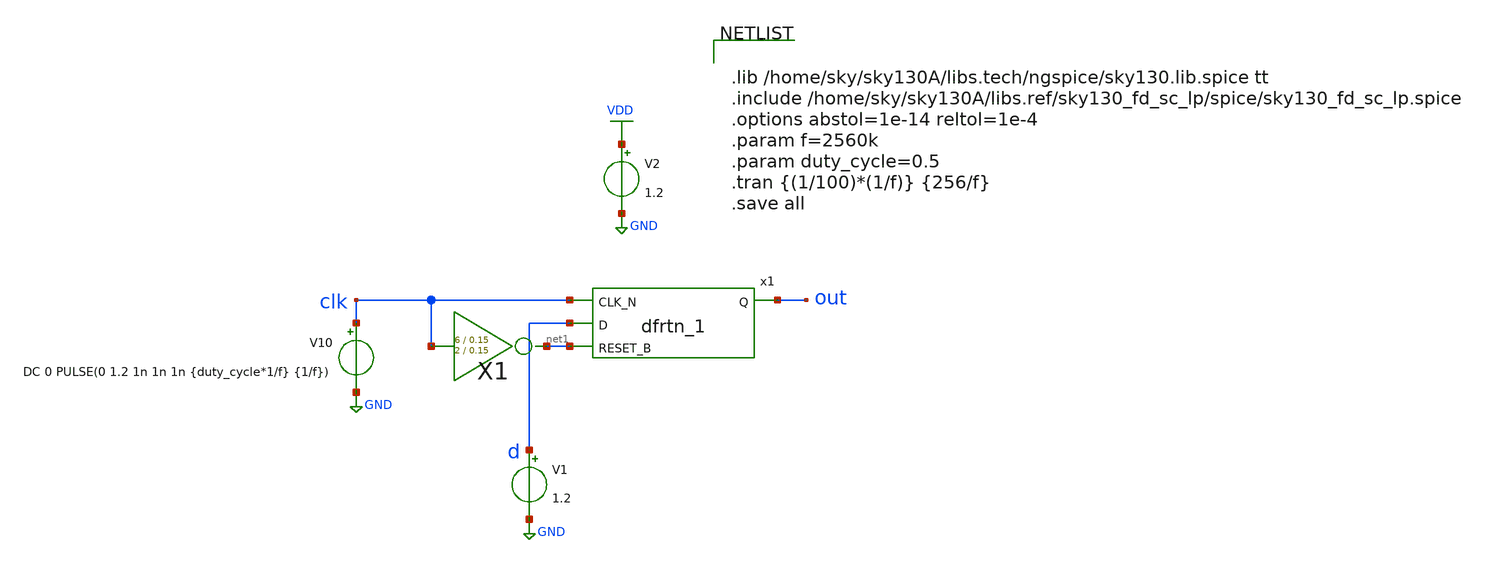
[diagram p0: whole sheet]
** sch_path: xschem/readout/test_flop.sch
**.subckt test_flop
V2 VDD GND 1.2
V10 clk GND DC 0 PULSE(0 1.2 1n 1n 1n {duty_cycle*1/f} {1/f})
V1 d GND 1.2
x1 clk d net1 GND GND VDD VDD out sky130_fd_sc_lp__dfrtn_1
X1 clk net1 inv Wpmos=6 Lpmos=0.15 Wnmos=2 Lnmos=0.15
**** begin user architecture code


.lib /home/sky/sky130A/libs.tech/ngspice/sky130.lib.spice tt
.include /home/sky/sky130A/libs.ref/sky130_fd_sc_lp/spice/sky130_fd_sc_lp.spice
.options abstol=1e-14 reltol=1e-4
.param f=2560k
.param duty_cycle=0.5
.tran {(1/100)*(1/f)} {256/f}
.save all


**** end user architecture code
**.ends

* expanding   symbol:  inv/inv.sym # of pins=2
** sym_path: xschem/inv/inv.sym
** sch_path: xschem/inv/inv.sch
.subckt inv in out  Wpmos=3 Lpmos=0.18 Wnmos=1 Lnmos=0.18
*.ipin in
*.iopin out
XM1 out in GND GND sky130_fd_pr__nfet_01v8 L=Lnmos W=Wnmos nf=1 ad='int((nf+1)/2) * W/nf * 0.29' as='int((nf+2)/2) * W/nf * 0.29'
+ pd='2*int((nf+1)/2) * (W/nf + 0.29)' ps='2*int((nf+2)/2) * (W/nf + 0.29)' nrd='0.29 / W' nrs='0.29 / W'
+ sa=0 sb=0 sd=0 mult=1 m=1
XM2 out in VDD VDD sky130_fd_pr__pfet_01v8 L=Lpmos W=Wpmos nf=1 ad='int((nf+1)/2) * W/nf * 0.29' as='int((nf+2)/2) * W/nf * 0.29'
+ pd='2*int((nf+1)/2) * (W/nf + 0.29)' ps='2*int((nf+2)/2) * (W/nf + 0.29)' nrd='0.29 / W' nrs='0.29 / W'
+ sa=0 sb=0 sd=0 mult=1 m=1
.ends

.GLOBAL GND
.GLOBAL VDD
.end
